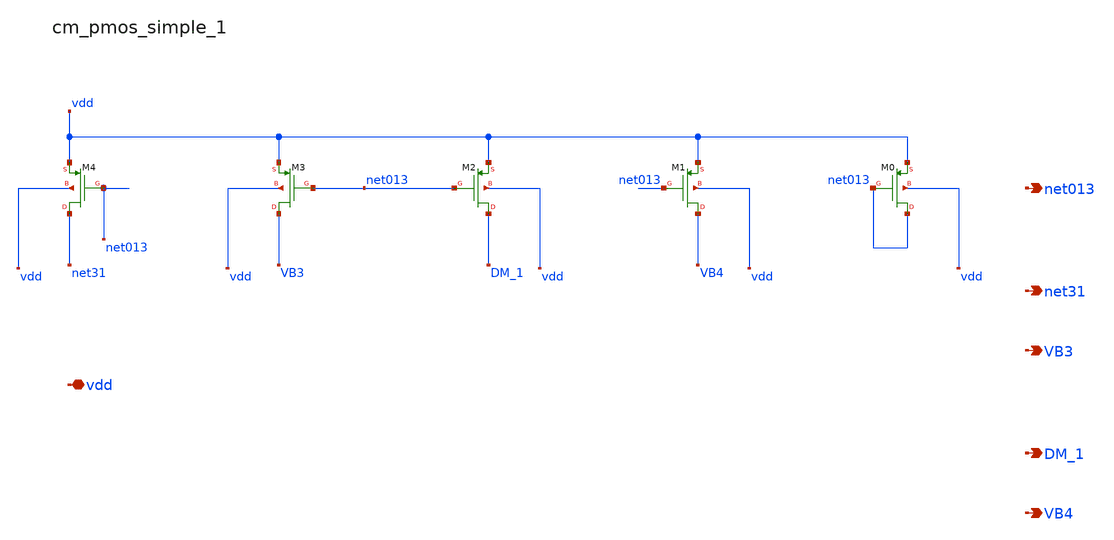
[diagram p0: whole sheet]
** sch_path: analog-db/raw/amp_015_sau_cfcc/hier/blocks/cm_pmos_simple_1.sch
**.subckt cm_pmos_simple_1 vdd net013 net31 VB3 DM_1 VB4
*.iopin vdd
*.opin net013
*.opin net31
*.opin VB3
*.opin DM_1
*.opin VB4
XM0 net013 net013 vdd vdd sg13_lv_pmos w=x_dut_xm0_w l=x_dut_xm0_l ng=1 m=x_dut_xm0_m
XM1 VB4 net013 vdd vdd sg13_lv_pmos w=x_dut_xm1_w l=x_dut_xm1_l ng=1 m=x_dut_xm1_m
XM2 DM_1 net013 vdd vdd sg13_lv_pmos w=x_dut_xm2_w l=x_dut_xm2_l ng=1 m=x_dut_xm2_m
XM3 VB3 net013 vdd vdd sg13_lv_pmos w=x_dut_xm3_w l=x_dut_xm3_l ng=1 m=x_dut_xm3_m
XM4 net31 net013 vdd vdd sg13_lv_pmos w=x_dut_xm4_w l=x_dut_xm4_l ng=1 m=x_dut_xm4_m
**.ends
.end
